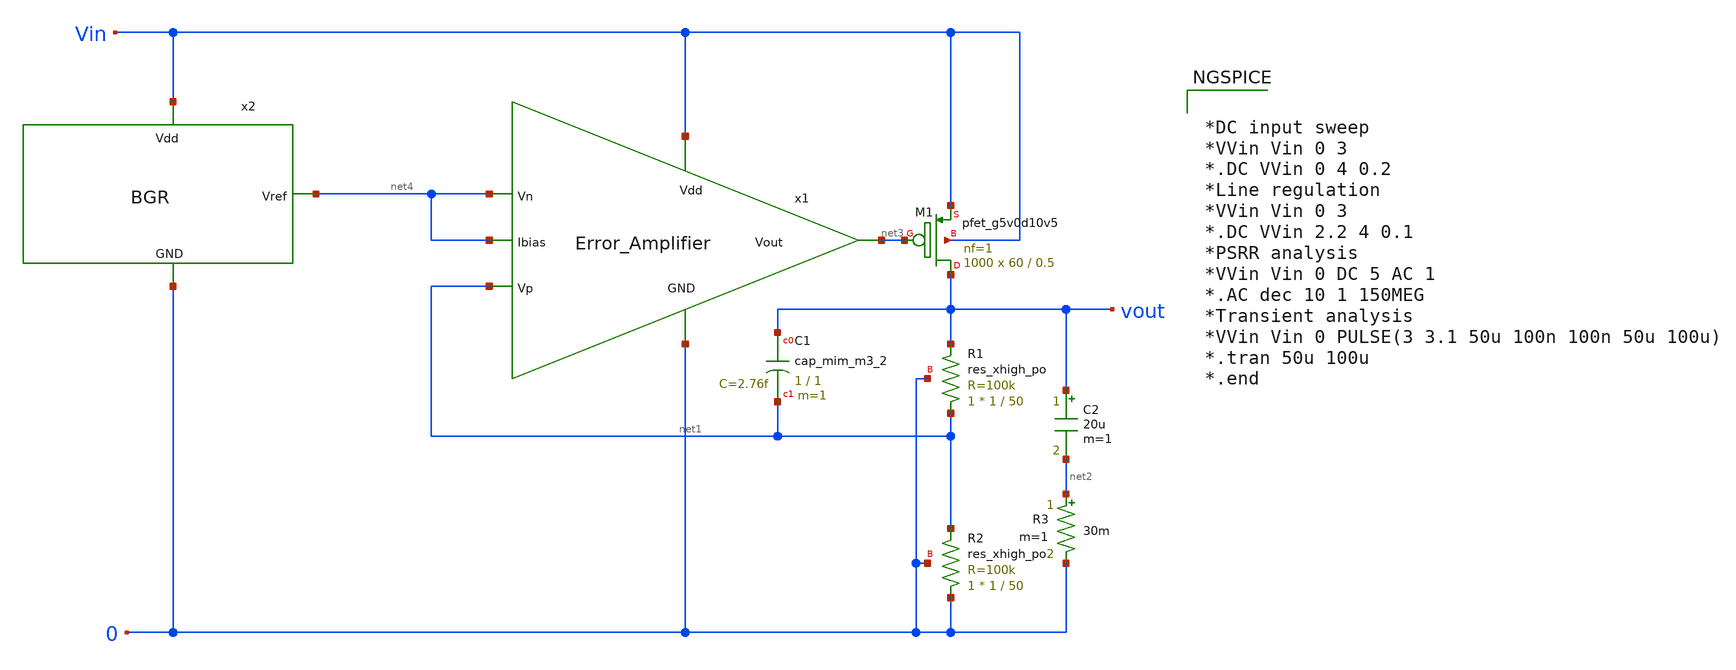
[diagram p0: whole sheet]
** sch_path: Analog_Blocks/LDO/Schematic/LDO_Miller_OTA_2.2v.sch
**.subckt LDO_Miller_OTA_2.2v
C2 vout net2 20u m=1
R3 net2 0 30m m=1
XR1 net1 vout 0 sky130_fd_pr__res_xhigh_po W=1 L=50 mult=1 m=1
XR2 0 net1 0 sky130_fd_pr__res_xhigh_po W=1 L=50 mult=1 m=1
XC1 vout net1 sky130_fd_pr__cap_mim_m3_2 W=1 L=1 MF=1 m=1
XM1 vout net3 Vin Vin sky130_fd_pr__pfet_g5v0d10v5 L=0.5 W=60 nf=1 ad='int((nf+1)/2) * W/nf * 0.29' as='int((nf+2)/2) * W/nf * 0.29'
+ pd='2*int((nf+1)/2) * (W/nf + 0.29)' ps='2*int((nf+2)/2) * (W/nf + 0.29)' nrd='0.29 / W' nrs='0.29 / W'
+ sa=0 sb=0 sd=0 mult=1000 m=1000
x1 Vin net4 net1 net3 net4 0 Error_Amplifier
x2 net4 Vin 0 BGR
**** begin user architecture code


*DC input sweep
*VVin Vin 0 3
*.DC VVin 0 4 0.2
*Line regulation
*VVin Vin 0 3
*.DC VVin 2.2 4 0.1
*PSRR analysis
*VVin Vin 0 DC 5 AC 1
*.AC dec 10 1 150MEG
*Transient analysis
*VVin Vin 0 PULSE(3 3.1 50u 100n 100n 50u 100u)
*.tran 50u 100u
*.end



.include $::SKYWATER_MODELS/cells/nfet_01v8/sky130_fd_pr__nfet_01v8__tt.corner.spice
.include $::SKYWATER_MODELS/cells/nfet_01v8_lvt/sky130_fd_pr__nfet_01v8_lvt__tt.corner.spice
.include $::SKYWATER_MODELS/cells/pfet_01v8/sky130_fd_pr__pfet_01v8__tt.corner.spice
.include $::SKYWATER_MODELS/cells/nfet_03v3_nvt/sky130_fd_pr__nfet_03v3_nvt__tt.corner.spice
.include $::SKYWATER_MODELS/cells/nfet_05v0_nvt/sky130_fd_pr__nfet_05v0_nvt__tt.corner.spice
.include $::SKYWATER_MODELS/cells/esd_nfet_01v8/sky130_fd_pr__esd_nfet_01v8__tt.corner.spice
.include $::SKYWATER_MODELS/cells/pfet_01v8_lvt/sky130_fd_pr__pfet_01v8_lvt__tt.corner.spice
.include $::SKYWATER_MODELS/cells/pfet_01v8_hvt/sky130_fd_pr__pfet_01v8_hvt__tt.corner.spice
.include $::SKYWATER_MODELS/cells/esd_pfet_g5v0d10v5/sky130_fd_pr__esd_pfet_g5v0d10v5__tt.corner.spice
.include $::SKYWATER_MODELS/cells/pfet_g5v0d10v5/sky130_fd_pr__pfet_g5v0d10v5__tt.corner.spice
.include $::SKYWATER_MODELS/cells/pfet_g5v0d16v0/sky130_fd_pr__pfet_g5v0d16v0__tt.corner.spice
.include $::SKYWATER_MODELS/cells/nfet_g5v0d10v5/sky130_fd_pr__nfet_g5v0d10v5__tt.corner.spice
.include $::SKYWATER_MODELS/cells/nfet_g5v0d16v0/sky130_fd_pr__nfet_g5v0d16v0__tt_discrete.corner.spice
.include $::SKYWATER_MODELS/cells/esd_nfet_g5v0d10v5/sky130_fd_pr__esd_nfet_g5v0d10v5__tt.corner.spice
.include $::SKYWATER_MODELS/models/corners/tt/nonfet.spice
* Mismatch parameters
.include $::SKYWATER_MODELS/cells/nfet_01v8/sky130_fd_pr__nfet_01v8__mismatch.corner.spice
.include $::SKYWATER_MODELS/cells/pfet_01v8/sky130_fd_pr__pfet_01v8__mismatch.corner.spice
.include $::SKYWATER_MODELS/cells/nfet_01v8_lvt/sky130_fd_pr__nfet_01v8_lvt__mismatch.corner.spice
.include $::SKYWATER_MODELS/cells/pfet_01v8_lvt/sky130_fd_pr__pfet_01v8_lvt__mismatch.corner.spice
.include $::SKYWATER_MODELS/cells/pfet_01v8_hvt/sky130_fd_pr__pfet_01v8_hvt__mismatch.corner.spice
.include $::SKYWATER_MODELS/cells/nfet_g5v0d10v5/sky130_fd_pr__nfet_g5v0d10v5__mismatch.corner.spice
.include $::SKYWATER_MODELS/cells/pfet_g5v0d10v5/sky130_fd_pr__pfet_g5v0d10v5__mismatch.corner.spice
.include $::SKYWATER_MODELS/cells/nfet_05v0_nvt/sky130_fd_pr__nfet_05v0_nvt__mismatch.corner.spice
.include $::SKYWATER_MODELS/cells/nfet_03v3_nvt/sky130_fd_pr__nfet_03v3_nvt__mismatch.corner.spice
* Resistor$::SKYWATER_MODELS/Capacitor
.include $::SKYWATER_MODELS/models/r+c/res_typical__cap_typical.spice
.include $::SKYWATER_MODELS/models/r+c/res_typical__cap_typical__lin.spice
* Special cells
.include $::SKYWATER_MODELS/models/corners/tt/specialized_cells.spice
* All models
.include $::SKYWATER_MODELS/models/all.spice
* Corner
.include $::SKYWATER_MODELS/models/corners/tt/rf.spice

**** end user architecture code
**.ends
.end
